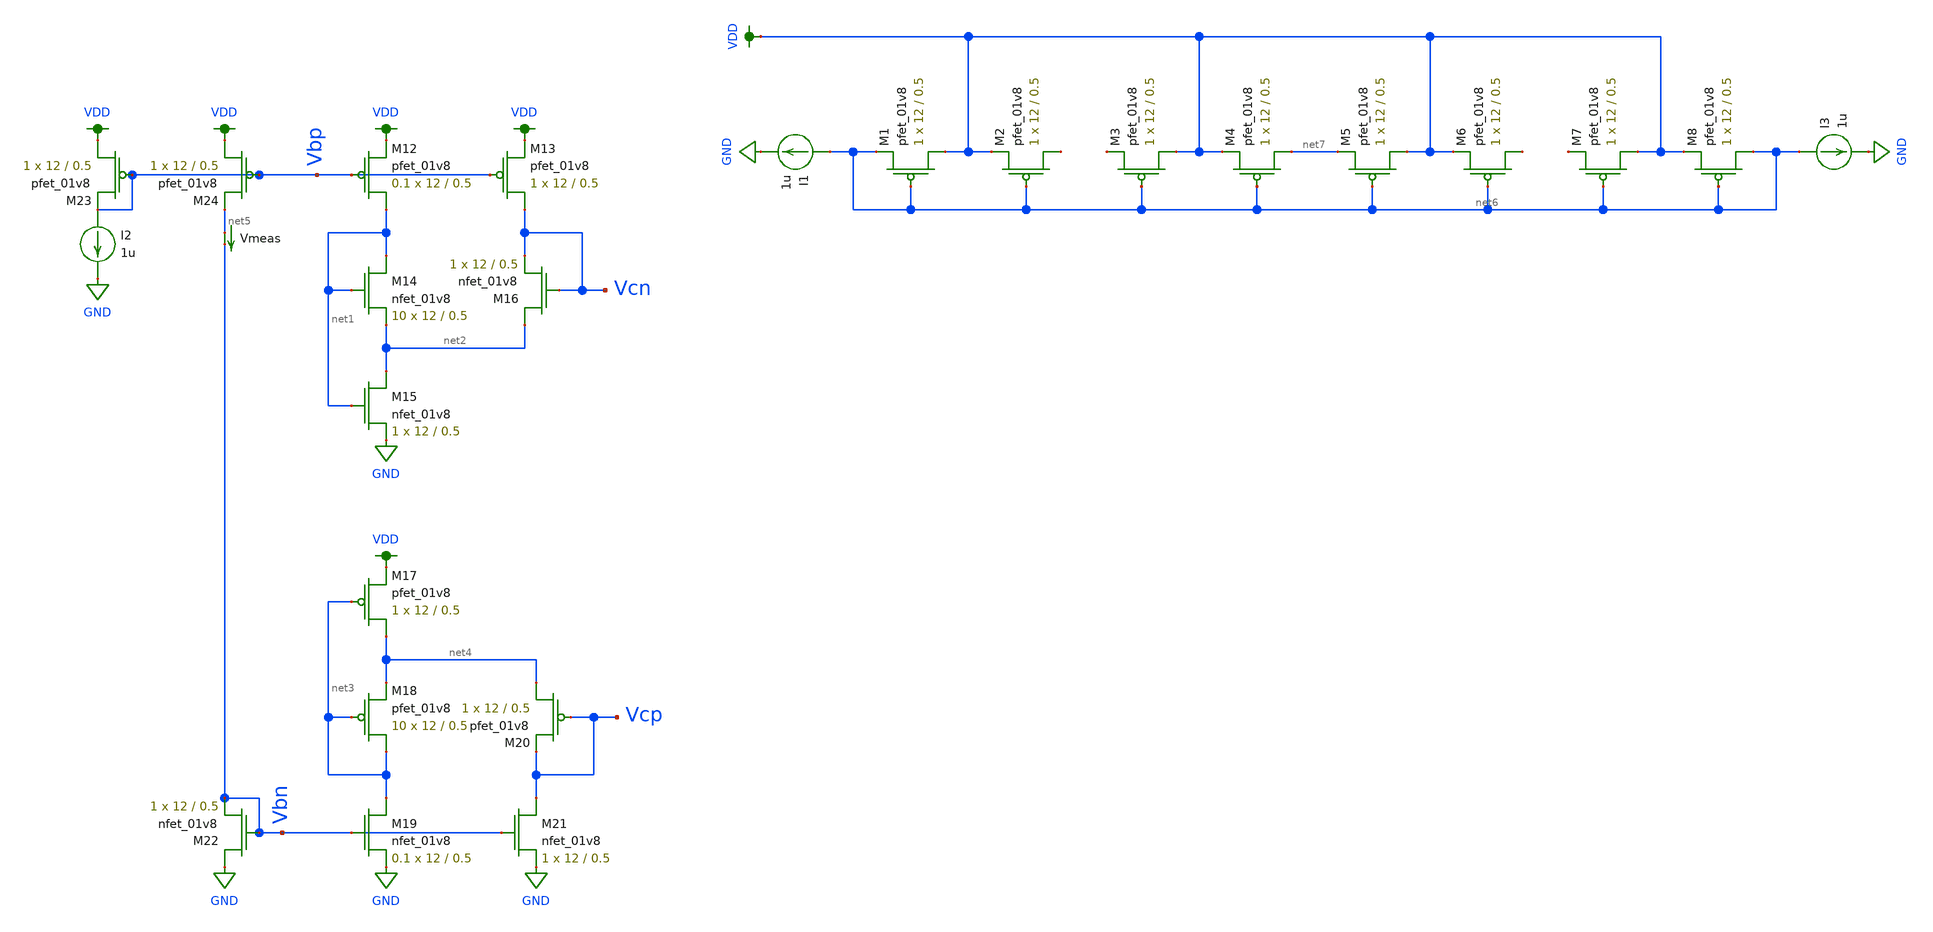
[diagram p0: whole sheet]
** sch_path: schematic/cascode_bias_LDS.sch
**.subckt cascode_bias_LDS
XM12 net1 Vbp VDD VDD sky130_fd_pr__pfet_01v8 L=0.5 W=12 nf=1 ad='int((nf+1)/2) * W/nf * 0.29' as='int((nf+2)/2) * W/nf * 0.29'
+ pd='2*int((nf+1)/2) * (W/nf + 0.29)' ps='2*int((nf+2)/2) * (W/nf + 0.29)' nrd='0.29 / W' nrs='0.29 / W'
+ sa=0 sb=0 sd=0 mult=0.1 m=0.1
XM13 Vcn Vbp VDD VDD sky130_fd_pr__pfet_01v8 L=0.5 W=12 nf=1 ad='int((nf+1)/2) * W/nf * 0.29' as='int((nf+2)/2) * W/nf * 0.29'
+ pd='2*int((nf+1)/2) * (W/nf + 0.29)' ps='2*int((nf+2)/2) * (W/nf + 0.29)' nrd='0.29 / W' nrs='0.29 / W'
+ sa=0 sb=0 sd=0 mult=1 m=1
XM14 net1 net1 net2 GND sky130_fd_pr__nfet_01v8 L=0.5 W=12 nf=1 ad='int((nf+1)/2) * W/nf * 0.29' as='int((nf+2)/2) * W/nf * 0.29'
+ pd='2*int((nf+1)/2) * (W/nf + 0.29)' ps='2*int((nf+2)/2) * (W/nf + 0.29)' nrd='0.29 / W' nrs='0.29 / W'
+ sa=0 sb=0 sd=0 mult=10 m=10
XM15 net2 net1 GND GND sky130_fd_pr__nfet_01v8 L=0.5 W=12 nf=1 ad='int((nf+1)/2) * W/nf * 0.29' as='int((nf+2)/2) * W/nf * 0.29'
+ pd='2*int((nf+1)/2) * (W/nf + 0.29)' ps='2*int((nf+2)/2) * (W/nf + 0.29)' nrd='0.29 / W' nrs='0.29 / W'
+ sa=0 sb=0 sd=0 mult=1 m=1
XM16 net2 Vcn Vcn GND sky130_fd_pr__nfet_01v8 L=0.5 W=12 nf=1 ad='int((nf+1)/2) * W/nf * 0.29' as='int((nf+2)/2) * W/nf * 0.29'
+ pd='2*int((nf+1)/2) * (W/nf + 0.29)' ps='2*int((nf+2)/2) * (W/nf + 0.29)' nrd='0.29 / W' nrs='0.29 / W'
+ sa=0 sb=0 sd=0 mult=1 m=1
XM17 net4 net3 VDD VDD sky130_fd_pr__pfet_01v8 L=0.5 W=12 nf=1 ad='int((nf+1)/2) * W/nf * 0.29' as='int((nf+2)/2) * W/nf * 0.29'
+ pd='2*int((nf+1)/2) * (W/nf + 0.29)' ps='2*int((nf+2)/2) * (W/nf + 0.29)' nrd='0.29 / W' nrs='0.29 / W'
+ sa=0 sb=0 sd=0 mult=1 m=1
XM18 net3 net3 net4 VDD sky130_fd_pr__pfet_01v8 L=0.5 W=12 nf=1 ad='int((nf+1)/2) * W/nf * 0.29' as='int((nf+2)/2) * W/nf * 0.29'
+ pd='2*int((nf+1)/2) * (W/nf + 0.29)' ps='2*int((nf+2)/2) * (W/nf + 0.29)' nrd='0.29 / W' nrs='0.29 / W'
+ sa=0 sb=0 sd=0 mult=10 m=10
XM19 net3 Vbn GND GND sky130_fd_pr__nfet_01v8 L=0.5 W=12 nf=1 ad='int((nf+1)/2) * W/nf * 0.29' as='int((nf+2)/2) * W/nf * 0.29'
+ pd='2*int((nf+1)/2) * (W/nf + 0.29)' ps='2*int((nf+2)/2) * (W/nf + 0.29)' nrd='0.29 / W' nrs='0.29 / W'
+ sa=0 sb=0 sd=0 mult=0.1 m=0.1
XM20 net4 Vcp Vcp VDD sky130_fd_pr__pfet_01v8 L=0.5 W=12 nf=1 ad='int((nf+1)/2) * W/nf * 0.29' as='int((nf+2)/2) * W/nf * 0.29'
+ pd='2*int((nf+1)/2) * (W/nf + 0.29)' ps='2*int((nf+2)/2) * (W/nf + 0.29)' nrd='0.29 / W' nrs='0.29 / W'
+ sa=0 sb=0 sd=0 mult=1 m=1
XM21 Vcp Vbn GND GND sky130_fd_pr__nfet_01v8 L=0.5 W=12 nf=1 ad='int((nf+1)/2) * W/nf * 0.29' as='int((nf+2)/2) * W/nf * 0.29'
+ pd='2*int((nf+1)/2) * (W/nf + 0.29)' ps='2*int((nf+2)/2) * (W/nf + 0.29)' nrd='0.29 / W' nrs='0.29 / W'
+ sa=0 sb=0 sd=0 mult=1 m=1
XM22 GND Vbn Vbn GND sky130_fd_pr__nfet_01v8 L=0.5 W=12 nf=1 ad='int((nf+1)/2) * W/nf * 0.29' as='int((nf+2)/2) * W/nf * 0.29'
+ pd='2*int((nf+1)/2) * (W/nf + 0.29)' ps='2*int((nf+2)/2) * (W/nf + 0.29)' nrd='0.29 / W' nrs='0.29 / W'
+ sa=0 sb=0 sd=0 mult=1 m=1
XM23 VDD Vbp Vbp VDD sky130_fd_pr__pfet_01v8 L=0.5 W=12 nf=1 ad='int((nf+1)/2) * W/nf * 0.29' as='int((nf+2)/2) * W/nf * 0.29'
+ pd='2*int((nf+1)/2) * (W/nf + 0.29)' ps='2*int((nf+2)/2) * (W/nf + 0.29)' nrd='0.29 / W' nrs='0.29 / W'
+ sa=0 sb=0 sd=0 mult=1 m=1
I2 Vbp GND 1u
XM24 VDD Vbp net5 VDD sky130_fd_pr__pfet_01v8 L=0.5 W=12 nf=1 ad='int((nf+1)/2) * W/nf * 0.29' as='int((nf+2)/2) * W/nf * 0.29'
+ pd='2*int((nf+1)/2) * (W/nf + 0.29)' ps='2*int((nf+2)/2) * (W/nf + 0.29)' nrd='0.29 / W' nrs='0.29 / W'
+ sa=0 sb=0 sd=0 mult=1 m=1
Vmeas net5 Vbn 0
.save i(vmeas)
XM1 VDD net6 net6 VDD sky130_fd_pr__pfet_01v8 L=0.5 W=12 nf=1 ad='int((nf+1)/2) * W/nf * 0.29' as='int((nf+2)/2) * W/nf * 0.29'
+ pd='2*int((nf+1)/2) * (W/nf + 0.29)' ps='2*int((nf+2)/2) * (W/nf + 0.29)' nrd='0.29 / W' nrs='0.29 / W'
+ sa=0 sb=0 sd=0 mult=1 m=1
XM2 net8 net6 VDD VDD sky130_fd_pr__pfet_01v8 L=0.5 W=12 nf=1 ad='int((nf+1)/2) * W/nf * 0.29' as='int((nf+2)/2) * W/nf * 0.29'
+ pd='2*int((nf+1)/2) * (W/nf + 0.29)' ps='2*int((nf+2)/2) * (W/nf + 0.29)' nrd='0.29 / W' nrs='0.29 / W'
+ sa=0 sb=0 sd=0 mult=1 m=1
XM3 VDD net6 net9 VDD sky130_fd_pr__pfet_01v8 L=0.5 W=12 nf=1 ad='int((nf+1)/2) * W/nf * 0.29' as='int((nf+2)/2) * W/nf * 0.29'
+ pd='2*int((nf+1)/2) * (W/nf + 0.29)' ps='2*int((nf+2)/2) * (W/nf + 0.29)' nrd='0.29 / W' nrs='0.29 / W'
+ sa=0 sb=0 sd=0 mult=1 m=1
XM4 net7 net6 VDD VDD sky130_fd_pr__pfet_01v8 L=0.5 W=12 nf=1 ad='int((nf+1)/2) * W/nf * 0.29' as='int((nf+2)/2) * W/nf * 0.29'
+ pd='2*int((nf+1)/2) * (W/nf + 0.29)' ps='2*int((nf+2)/2) * (W/nf + 0.29)' nrd='0.29 / W' nrs='0.29 / W'
+ sa=0 sb=0 sd=0 mult=1 m=1
I1 net6 GND 1u
XM5 VDD net6 net7 VDD sky130_fd_pr__pfet_01v8 L=0.5 W=12 nf=1 ad='int((nf+1)/2) * W/nf * 0.29' as='int((nf+2)/2) * W/nf * 0.29'
+ pd='2*int((nf+1)/2) * (W/nf + 0.29)' ps='2*int((nf+2)/2) * (W/nf + 0.29)' nrd='0.29 / W' nrs='0.29 / W'
+ sa=0 sb=0 sd=0 mult=1 m=1
XM6 net10 net6 VDD VDD sky130_fd_pr__pfet_01v8 L=0.5 W=12 nf=1 ad='int((nf+1)/2) * W/nf * 0.29' as='int((nf+2)/2) * W/nf * 0.29'
+ pd='2*int((nf+1)/2) * (W/nf + 0.29)' ps='2*int((nf+2)/2) * (W/nf + 0.29)' nrd='0.29 / W' nrs='0.29 / W'
+ sa=0 sb=0 sd=0 mult=1 m=1
XM7 VDD net6 net11 VDD sky130_fd_pr__pfet_01v8 L=0.5 W=12 nf=1 ad='int((nf+1)/2) * W/nf * 0.29' as='int((nf+2)/2) * W/nf * 0.29'
+ pd='2*int((nf+1)/2) * (W/nf + 0.29)' ps='2*int((nf+2)/2) * (W/nf + 0.29)' nrd='0.29 / W' nrs='0.29 / W'
+ sa=0 sb=0 sd=0 mult=1 m=1
XM8 net6 net6 VDD VDD sky130_fd_pr__pfet_01v8 L=0.5 W=12 nf=1 ad='int((nf+1)/2) * W/nf * 0.29' as='int((nf+2)/2) * W/nf * 0.29'
+ pd='2*int((nf+1)/2) * (W/nf + 0.29)' ps='2*int((nf+2)/2) * (W/nf + 0.29)' nrd='0.29 / W' nrs='0.29 / W'
+ sa=0 sb=0 sd=0 mult=1 m=1
I3 net6 GND 1u
**.ends
.GLOBAL GND
.GLOBAL VDD
.end
